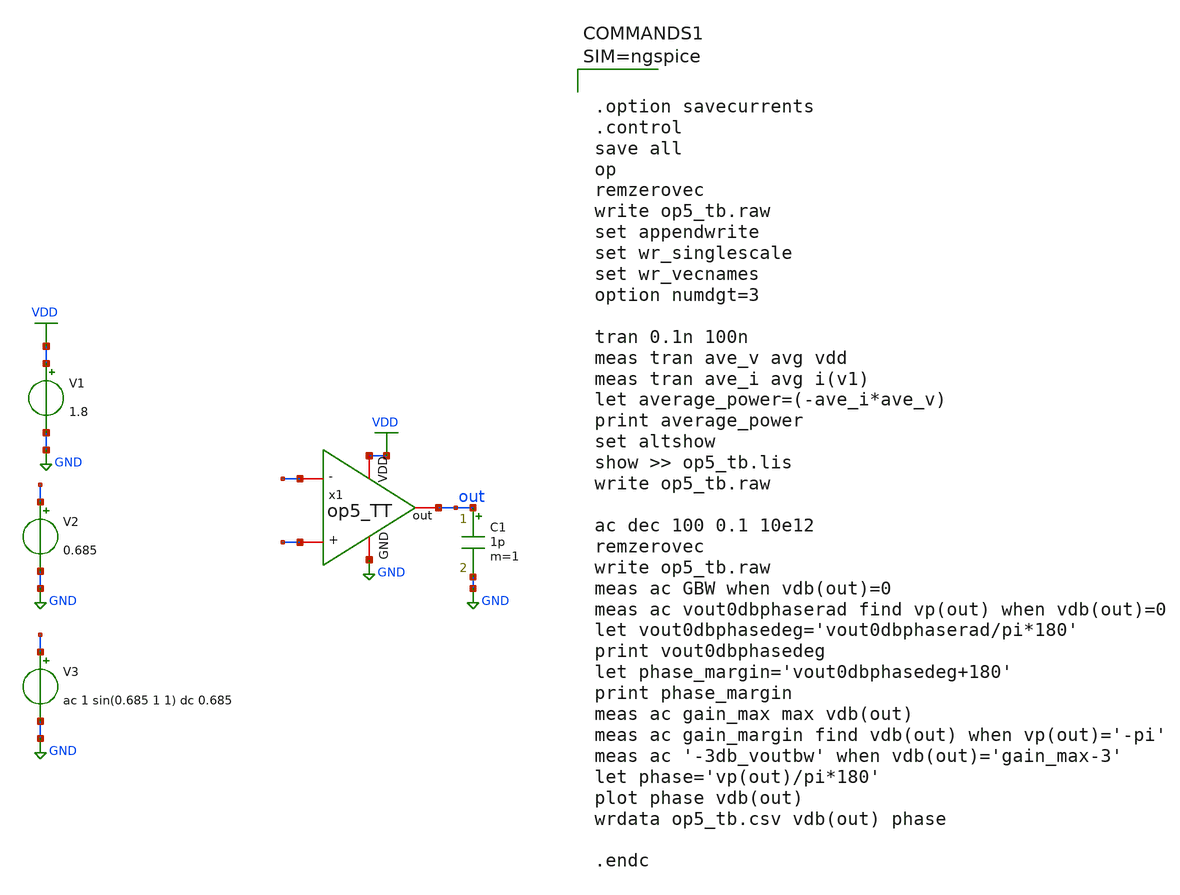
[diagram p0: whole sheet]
** sch_path: xschem/op5_tb.sch
**.subckt op5_tb
V1 VDD GND 1.8
V2 - GND 0.685
V3 + GND ac 1 sin(0.685 1 1) dc 0.685
C1 out GND 1p m=1
x1 VDD out - + GND op5_TT
**** begin user architecture code

** opencircuitdesign pdks install
.lib $::SKYWATER_MODELS/sky130.lib.spice tt





.option savecurrents
.control
save all
op
remzerovec
write op5_tb.raw
set appendwrite
set wr_singlescale
set wr_vecnames
option numdgt=3

tran 0.1n 100n
meas tran ave_v avg vdd
meas tran ave_i avg i(v1)
let average_power=(-ave_i*ave_v)
print average_power
set altshow
show >> op5_tb.lis
write op5_tb.raw

ac dec 100 0.1 10e12
remzerovec
write op5_tb.raw
meas ac GBW when vdb(out)=0
meas ac vout0dbphaserad find vp(out) when vdb(out)=0
let vout0dbphasedeg='vout0dbphaserad/pi*180'
print vout0dbphasedeg
let phase_margin='vout0dbphasedeg+180'
print phase_margin
meas ac gain_max max vdb(out)
meas ac gain_margin find vdb(out) when vp(out)='-pi'
meas ac '-3db_voutbw' when vdb(out)='gain_max-3'
let phase='vp(out)/pi*180'
plot phase vdb(out)
wrdata op5_tb.csv vdb(out) phase

.endc



**** end user architecture code
**.ends

* expanding   symbol:  /home/gilang_fajrul/chipalooza/sky130_gff_ip__bgr_1.2v/xschem/op5_TT.sym # of
*+ pins=5
** sym_path: xschem/op5_TT.sym
** sch_path: xschem/op5_TT.sch
.subckt op5_TT VDD out - + GND
*.iopin GND
*.iopin -
*.iopin +
*.iopin VDD
*.iopin out
XM8 net1 net2 VDD VDD sky130_fd_pr__pfet_01v8 L={L7} W={W7} nf=1 ad='int((nf+1)/2) * W/nf * 0.29' as='int((nf+2)/2) * W/nf * 0.29'
+ pd='2*int((nf+1)/2) * (W/nf + 0.29)' ps='2*int((nf+2)/2) * (W/nf + 0.29)' nrd='0.29 / W' nrs='0.29 / W'
+ sa=0 sb=0 sd=0 mult=4 m=4
XM9 net2 net2 VDD VDD sky130_fd_pr__pfet_01v8 L={L7} W={W7} nf=1 ad='int((nf+1)/2) * W/nf * 0.29' as='int((nf+2)/2) * W/nf * 0.29'
+ pd='2*int((nf+1)/2) * (W/nf + 0.29)' ps='2*int((nf+2)/2) * (W/nf + 0.29)' nrd='0.29 / W' nrs='0.29 / W'
+ sa=0 sb=0 sd=0 mult=4 m=4
XM5 net3 bias GND GND sky130_fd_pr__nfet_01v8 L={L6} W={W6} nf=1 ad='int((nf+1)/2) * W/nf * 0.29' as='int((nf+2)/2) * W/nf * 0.29'
+ pd='2*int((nf+1)/2) * (W/nf + 0.29)' ps='2*int((nf+2)/2) * (W/nf + 0.29)' nrd='0.29 / W' nrs='0.29 / W'
+ sa=0 sb=0 sd=0 mult=2 m=2
XM10 out net1 VDD VDD sky130_fd_pr__pfet_01v8 L={L2} W={W2} nf=1 ad='int((nf+1)/2) * W/nf * 0.29' as='int((nf+2)/2) * W/nf * 0.29'
+ pd='2*int((nf+1)/2) * (W/nf + 0.29)' ps='2*int((nf+2)/2) * (W/nf + 0.29)' nrd='0.29 / W' nrs='0.29 / W'
+ sa=0 sb=0 sd=0 mult=4 m=4
**** begin user architecture code


**************
*PMOS cms
.param L1=3
.param W1=1

**************
*PMOS current differential
.param L7=10
.param W7=1

**************
*differential Pair
.param L4=10
.param W4=1.2

**************
*NMOS current control
.param L6=20
.param W6=1

**************
*Second Stage
.param L2=10
.param W2=1


**** end user architecture code
XM11 out bias GND GND sky130_fd_pr__nfet_01v8 L={L6} W={W6} nf=1 ad='int((nf+1)/2) * W/nf * 0.29' as='int((nf+2)/2) * W/nf * 0.29'
+ pd='2*int((nf+1)/2) * (W/nf + 0.29)' ps='2*int((nf+2)/2) * (W/nf + 0.29)' nrd='0.29 / W' nrs='0.29 / W'
+ sa=0 sb=0 sd=0 mult=2 m=2
XM3 net1 + net3 GND sky130_fd_pr__nfet_01v8 L={L4} W={W4} nf=1 ad='int((nf+1)/2) * W/nf * 0.29' as='int((nf+2)/2) * W/nf * 0.29'
+ pd='2*int((nf+1)/2) * (W/nf + 0.29)' ps='2*int((nf+2)/2) * (W/nf + 0.29)' nrd='0.29 / W' nrs='0.29 / W'
+ sa=0 sb=0 sd=0 mult=2 m=2
XM1 bias net6 VDD VDD sky130_fd_pr__pfet_01v8 L={L1} W={W1} nf=1 ad='int((nf+1)/2) * W/nf * 0.29' as='int((nf+2)/2) * W/nf * 0.29'
+ pd='2*int((nf+1)/2) * (W/nf + 0.29)' ps='2*int((nf+2)/2) * (W/nf + 0.29)' nrd='0.29 / W' nrs='0.29 / W'
+ sa=0 sb=0 sd=0 mult=2 m=2
XM2 net6 net6 VDD VDD sky130_fd_pr__pfet_01v8 L={L1} W={W1} nf=1 ad='int((nf+1)/2) * W/nf * 0.29' as='int((nf+2)/2) * W/nf * 0.29'
+ pd='2*int((nf+1)/2) * (W/nf + 0.29)' ps='2*int((nf+2)/2) * (W/nf + 0.29)' nrd='0.29 / W' nrs='0.29 / W'
+ sa=0 sb=0 sd=0 mult=2 m=2
XM6 net6 bias net7 GND sky130_fd_pr__nfet_01v8 L={L6} W={W6} nf=1 ad='int((nf+1)/2) * W/nf * 0.29' as='int((nf+2)/2) * W/nf * 0.29'
+ pd='2*int((nf+1)/2) * (W/nf + 0.29)' ps='2*int((nf+2)/2) * (W/nf + 0.29)' nrd='0.29 / W' nrs='0.29 / W'
+ sa=0 sb=0 sd=0 mult=2 m=2
XM7 bias bias GND GND sky130_fd_pr__nfet_01v8 L={L6} W={W6} nf=1 ad='int((nf+1)/2) * W/nf * 0.29' as='int((nf+2)/2) * W/nf * 0.29'
+ pd='2*int((nf+1)/2) * (W/nf + 0.29)' ps='2*int((nf+2)/2) * (W/nf + 0.29)' nrd='0.29 / W' nrs='0.29 / W'
+ sa=0 sb=0 sd=0 mult=2 m=2
XR4 net7 GND GND sky130_fd_pr__res_high_po_0p35 L=3 mult=4 m=4
XM4 net2 - net3 GND sky130_fd_pr__nfet_01v8 L={L4} W={W4} nf=1 ad='int((nf+1)/2) * W/nf * 0.29' as='int((nf+2)/2) * W/nf * 0.29'
+ pd='2*int((nf+1)/2) * (W/nf + 0.29)' ps='2*int((nf+2)/2) * (W/nf + 0.29)' nrd='0.29 / W' nrs='0.29 / W'
+ sa=0 sb=0 sd=0 mult=2 m=2
XR1 net1 net4 GND sky130_fd_pr__res_high_po_0p35 L=3 mult=2 m=2
XR2 net4 net5 GND sky130_fd_pr__res_high_po_0p35 L=3 mult=2 m=2
XC1 out net5 sky130_fd_pr__cap_mim_m3_1 W=17 L=17 MF=4 m=4
.ends

.GLOBAL VDD
.GLOBAL GND
.end
